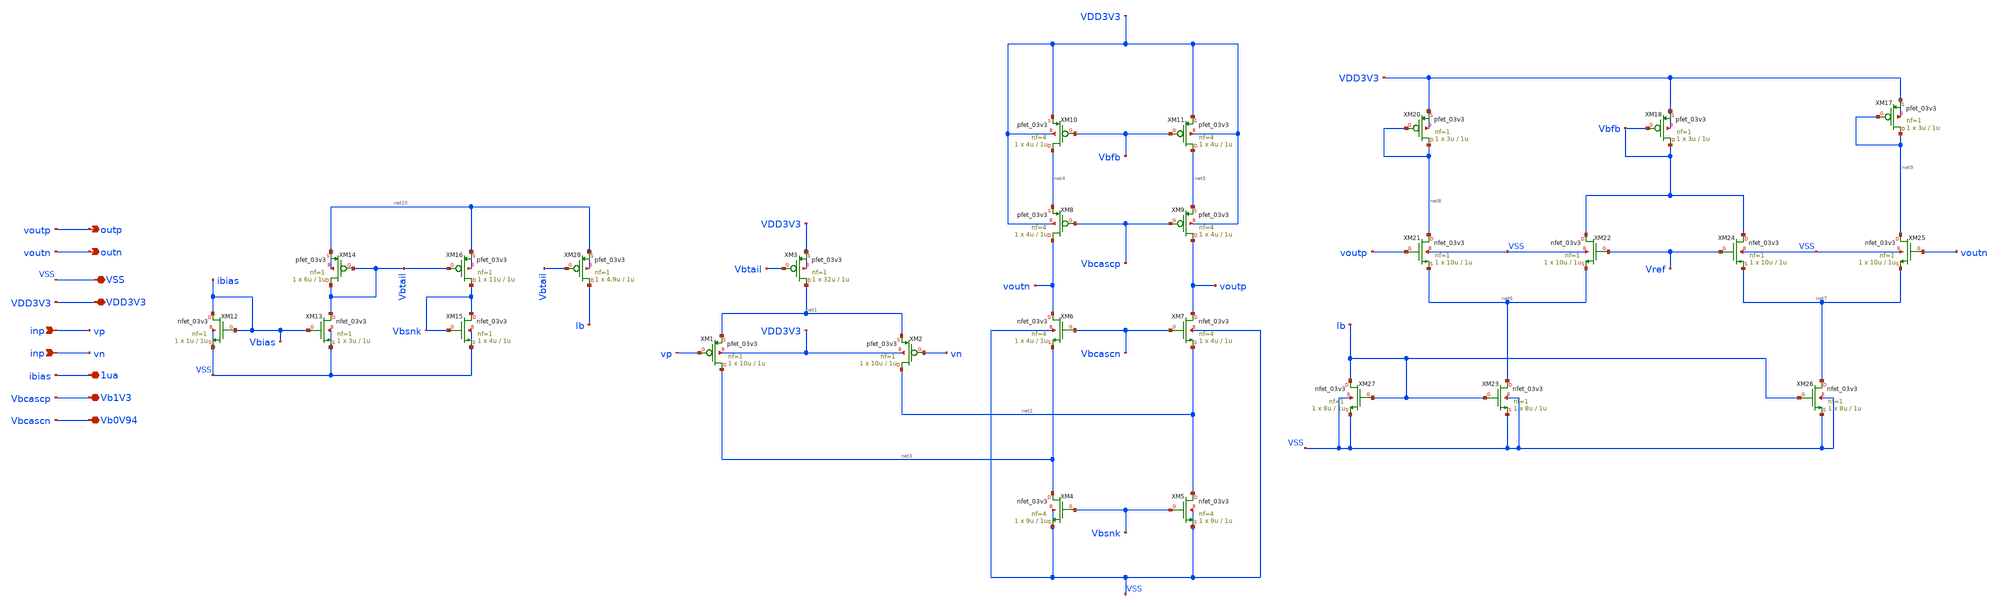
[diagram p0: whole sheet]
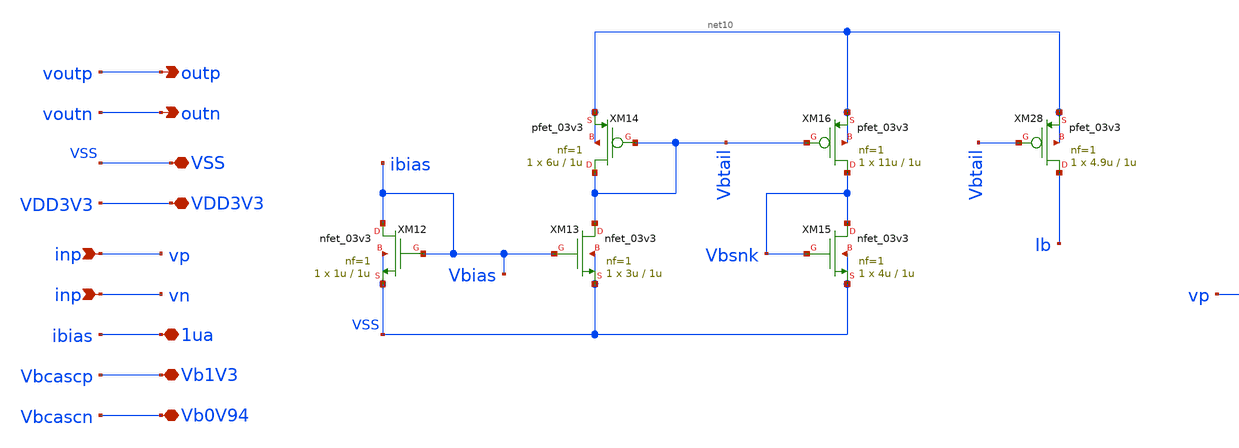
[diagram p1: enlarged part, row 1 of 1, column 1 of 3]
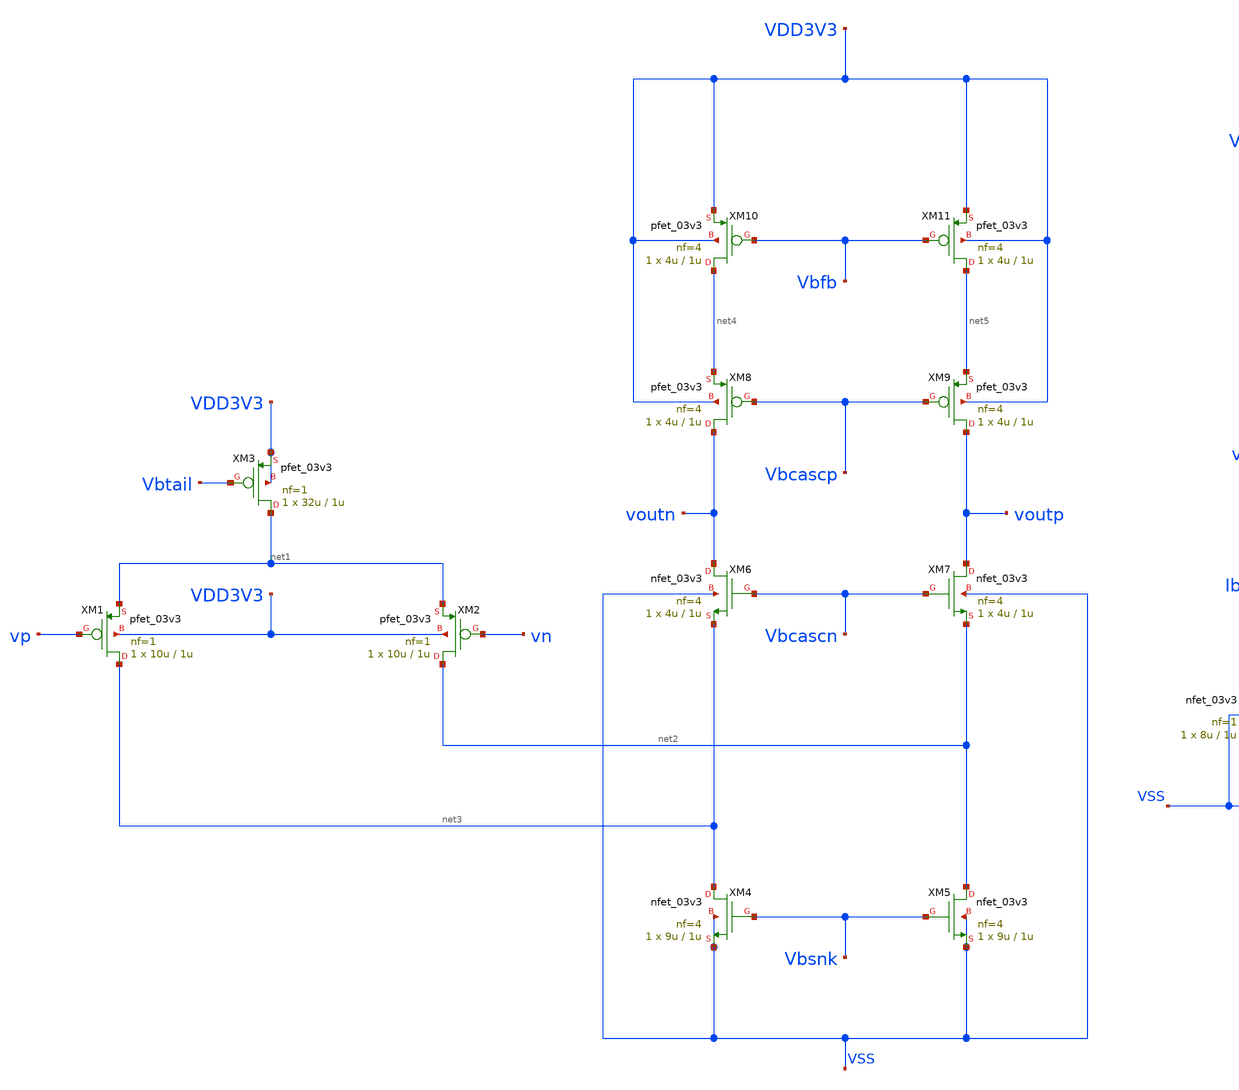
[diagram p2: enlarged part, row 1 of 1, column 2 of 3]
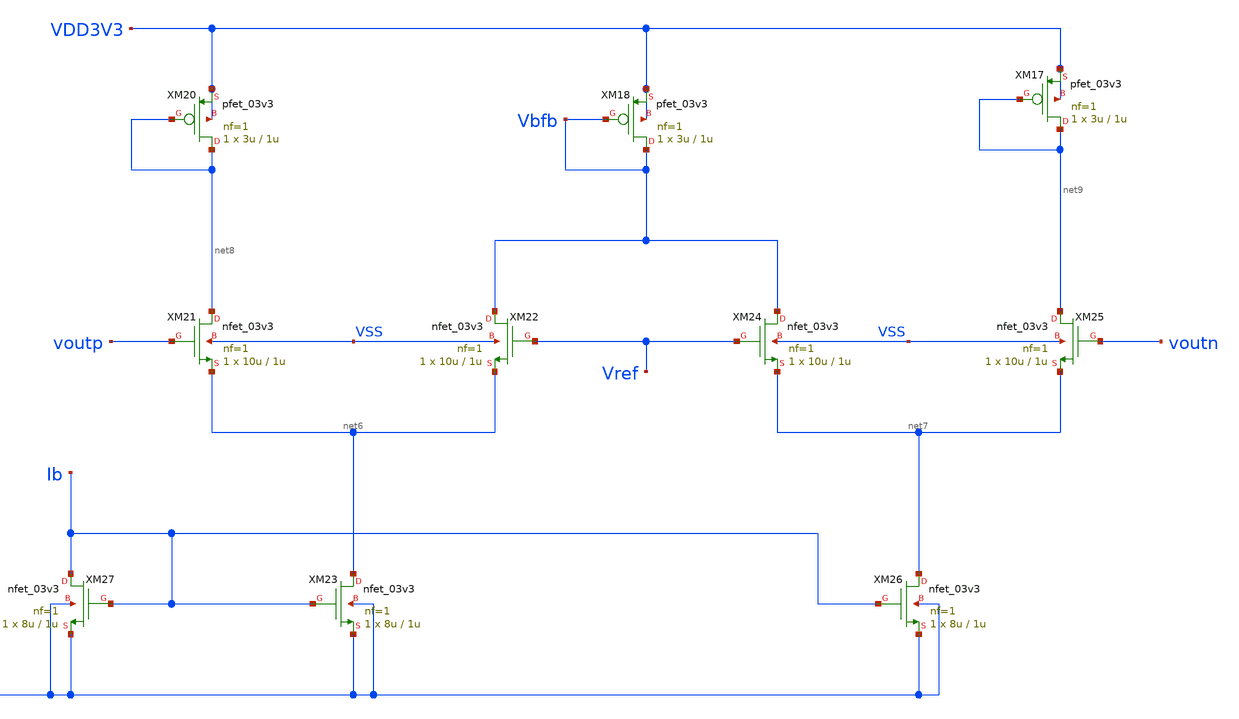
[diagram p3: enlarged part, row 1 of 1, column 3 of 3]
** sch_path: designs/libs/folded_cascode/folded_cascode_v2.sch
**.subckt folded_cascode_v2 outp outn VSS VDD3V3 inp inp 1ua Vb1V3 Vb0V94
*.opin outp
*.opin outn
*.iopin VSS
*.iopin VDD3V3
*.ipin inp
*.ipin inp
*.iopin 1ua
*.iopin Vb1V3
*.iopin Vb0V94
XM1 net3 vp net1 VDD3V3 pfet_03v3 L=1u W=10u nf=1 ad='int((nf+1)/2) * W/nf * 0.18u' as='int((nf+2)/2) * W/nf * 0.18u'
+ pd='2*int((nf+1)/2) * (W/nf + 0.18u)' ps='2*int((nf+2)/2) * (W/nf + 0.18u)' nrd='0.18u / W' nrs='0.18u / W'
+ sa=0 sb=0 sd=0 m=1
XM2 net2 vn net1 VDD3V3 pfet_03v3 L=1u W=10u nf=1 ad='int((nf+1)/2) * W/nf * 0.18u' as='int((nf+2)/2) * W/nf * 0.18u'
+ pd='2*int((nf+1)/2) * (W/nf + 0.18u)' ps='2*int((nf+2)/2) * (W/nf + 0.18u)' nrd='0.18u / W' nrs='0.18u / W'
+ sa=0 sb=0 sd=0 m=1
XM6 voutn Vbcascn net3 VSS nfet_03v3 L=1u W=4u nf=4 ad='int((nf+1)/2) * W/nf * 0.18u' as='int((nf+2)/2) * W/nf * 0.18u'
+ pd='2*int((nf+1)/2) * (W/nf + 0.18u)' ps='2*int((nf+2)/2) * (W/nf + 0.18u)' nrd='0.18u / W' nrs='0.18u / W'
+ sa=0 sb=0 sd=0 m=1
XM7 voutp Vbcascn net2 VSS nfet_03v3 L=1u W=4u nf=4 ad='int((nf+1)/2) * W/nf * 0.18u' as='int((nf+2)/2) * W/nf * 0.18u'
+ pd='2*int((nf+1)/2) * (W/nf + 0.18u)' ps='2*int((nf+2)/2) * (W/nf + 0.18u)' nrd='0.18u / W' nrs='0.18u / W'
+ sa=0 sb=0 sd=0 m=1
XM8 voutn Vbcascp net4 VDD3V3 pfet_03v3 L=1u W=4u nf=4 ad='int((nf+1)/2) * W/nf * 0.18u' as='int((nf+2)/2) * W/nf * 0.18u'
+ pd='2*int((nf+1)/2) * (W/nf + 0.18u)' ps='2*int((nf+2)/2) * (W/nf + 0.18u)' nrd='0.18u / W' nrs='0.18u / W'
+ sa=0 sb=0 sd=0 m=1
XM9 voutp Vbcascp net5 VDD3V3 pfet_03v3 L=1u W=4u nf=4 ad='int((nf+1)/2) * W/nf * 0.18u' as='int((nf+2)/2) * W/nf * 0.18u'
+ pd='2*int((nf+1)/2) * (W/nf + 0.18u)' ps='2*int((nf+2)/2) * (W/nf + 0.18u)' nrd='0.18u / W' nrs='0.18u / W'
+ sa=0 sb=0 sd=0 m=1
XM3 net1 Vbtail VDD3V3 VDD3V3 pfet_03v3 L=1u W=32u nf=1 ad='int((nf+1)/2) * W/nf * 0.18u' as='int((nf+2)/2) * W/nf * 0.18u'
+ pd='2*int((nf+1)/2) * (W/nf + 0.18u)' ps='2*int((nf+2)/2) * (W/nf + 0.18u)' nrd='0.18u / W' nrs='0.18u / W'
+ sa=0 sb=0 sd=0 m=1
XM4 net3 Vbsnk VSS VSS nfet_03v3 L=1u W=9u nf=4 ad='int((nf+1)/2) * W/nf * 0.18u' as='int((nf+2)/2) * W/nf * 0.18u'
+ pd='2*int((nf+1)/2) * (W/nf + 0.18u)' ps='2*int((nf+2)/2) * (W/nf + 0.18u)' nrd='0.18u / W' nrs='0.18u / W'
+ sa=0 sb=0 sd=0 m=1
XM5 net2 Vbsnk VSS VSS nfet_03v3 L=1u W=9u nf=4 ad='int((nf+1)/2) * W/nf * 0.18u' as='int((nf+2)/2) * W/nf * 0.18u'
+ pd='2*int((nf+1)/2) * (W/nf + 0.18u)' ps='2*int((nf+2)/2) * (W/nf + 0.18u)' nrd='0.18u / W' nrs='0.18u / W'
+ sa=0 sb=0 sd=0 m=1
XM10 net4 Vbfb VDD3V3 VDD3V3 pfet_03v3 L=1u W=4u nf=4 ad='int((nf+1)/2) * W/nf * 0.18u' as='int((nf+2)/2) * W/nf * 0.18u'
+ pd='2*int((nf+1)/2) * (W/nf + 0.18u)' ps='2*int((nf+2)/2) * (W/nf + 0.18u)' nrd='0.18u / W' nrs='0.18u / W'
+ sa=0 sb=0 sd=0 m=1
XM11 net5 Vbfb VDD3V3 VDD3V3 pfet_03v3 L=1u W=4u nf=4 ad='int((nf+1)/2) * W/nf * 0.18u' as='int((nf+2)/2) * W/nf * 0.18u'
+ pd='2*int((nf+1)/2) * (W/nf + 0.18u)' ps='2*int((nf+2)/2) * (W/nf + 0.18u)' nrd='0.18u / W' nrs='0.18u / W'
+ sa=0 sb=0 sd=0 m=1
XM20 net8 net8 VDD3V3 VDD3V3 pfet_03v3 L=1u W=3u nf=1 ad='int((nf+1)/2) * W/nf * 0.18u' as='int((nf+2)/2) * W/nf * 0.18u'
+ pd='2*int((nf+1)/2) * (W/nf + 0.18u)' ps='2*int((nf+2)/2) * (W/nf + 0.18u)' nrd='0.18u / W' nrs='0.18u / W'
+ sa=0 sb=0 sd=0 m=1
XM21 net8 voutp net6 VSS nfet_03v3 L=1u W=10u nf=1 ad='int((nf+1)/2) * W/nf * 0.18u' as='int((nf+2)/2) * W/nf * 0.18u'
+ pd='2*int((nf+1)/2) * (W/nf + 0.18u)' ps='2*int((nf+2)/2) * (W/nf + 0.18u)' nrd='0.18u / W' nrs='0.18u / W'
+ sa=0 sb=0 sd=0 m=1
XM22 Vbfb Vref net6 VSS nfet_03v3 L=1u W=10u nf=1 ad='int((nf+1)/2) * W/nf * 0.18u' as='int((nf+2)/2) * W/nf * 0.18u'
+ pd='2*int((nf+1)/2) * (W/nf + 0.18u)' ps='2*int((nf+2)/2) * (W/nf + 0.18u)' nrd='0.18u / W' nrs='0.18u / W'
+ sa=0 sb=0 sd=0 m=1
XM23 net6 Ib VSS VSS nfet_03v3 L=1u W=8u nf=1 ad='int((nf+1)/2) * W/nf * 0.18u' as='int((nf+2)/2) * W/nf * 0.18u'
+ pd='2*int((nf+1)/2) * (W/nf + 0.18u)' ps='2*int((nf+2)/2) * (W/nf + 0.18u)' nrd='0.18u / W' nrs='0.18u / W'
+ sa=0 sb=0 sd=0 m=1
XM24 Vbfb Vref net7 VSS nfet_03v3 L=1u W=10u nf=1 ad='int((nf+1)/2) * W/nf * 0.18u' as='int((nf+2)/2) * W/nf * 0.18u'
+ pd='2*int((nf+1)/2) * (W/nf + 0.18u)' ps='2*int((nf+2)/2) * (W/nf + 0.18u)' nrd='0.18u / W' nrs='0.18u / W'
+ sa=0 sb=0 sd=0 m=1
XM25 net9 voutn net7 VSS nfet_03v3 L=1u W=10u nf=1 ad='int((nf+1)/2) * W/nf * 0.18u' as='int((nf+2)/2) * W/nf * 0.18u'
+ pd='2*int((nf+1)/2) * (W/nf + 0.18u)' ps='2*int((nf+2)/2) * (W/nf + 0.18u)' nrd='0.18u / W' nrs='0.18u / W'
+ sa=0 sb=0 sd=0 m=1
XM26 net7 Ib VSS VSS nfet_03v3 L=1u W=8u nf=1 ad='int((nf+1)/2) * W/nf * 0.18u' as='int((nf+2)/2) * W/nf * 0.18u'
+ pd='2*int((nf+1)/2) * (W/nf + 0.18u)' ps='2*int((nf+2)/2) * (W/nf + 0.18u)' nrd='0.18u / W' nrs='0.18u / W'
+ sa=0 sb=0 sd=0 m=1
XM27 Ib Ib VSS VSS nfet_03v3 L=1u W=8u nf=1 ad='int((nf+1)/2) * W/nf * 0.18u' as='int((nf+2)/2) * W/nf * 0.18u'
+ pd='2*int((nf+1)/2) * (W/nf + 0.18u)' ps='2*int((nf+2)/2) * (W/nf + 0.18u)' nrd='0.18u / W' nrs='0.18u / W'
+ sa=0 sb=0 sd=0 m=1
XM12 Vbias Vbias VSS VSS nfet_03v3 L=1u W=1u nf=1 ad='int((nf+1)/2) * W/nf * 0.18u' as='int((nf+2)/2) * W/nf * 0.18u'
+ pd='2*int((nf+1)/2) * (W/nf + 0.18u)' ps='2*int((nf+2)/2) * (W/nf + 0.18u)' nrd='0.18u / W' nrs='0.18u / W'
+ sa=0 sb=0 sd=0 m=1
XM13 Vbtail Vbias VSS VSS nfet_03v3 L=1u W=3u nf=1 ad='int((nf+1)/2) * W/nf * 0.18u' as='int((nf+2)/2) * W/nf * 0.18u'
+ pd='2*int((nf+1)/2) * (W/nf + 0.18u)' ps='2*int((nf+2)/2) * (W/nf + 0.18u)' nrd='0.18u / W' nrs='0.18u / W'
+ sa=0 sb=0 sd=0 m=1
XM14 Vbtail Vbtail net10 net10 pfet_03v3 L=1u W=6u nf=1 ad='int((nf+1)/2) * W/nf * 0.18u' as='int((nf+2)/2) * W/nf * 0.18u'
+ pd='2*int((nf+1)/2) * (W/nf + 0.18u)' ps='2*int((nf+2)/2) * (W/nf + 0.18u)' nrd='0.18u / W' nrs='0.18u / W'
+ sa=0 sb=0 sd=0 m=1
XM15 Vbsnk Vbsnk VSS VSS nfet_03v3 L=1u W=4u nf=1 ad='int((nf+1)/2) * W/nf * 0.18u' as='int((nf+2)/2) * W/nf * 0.18u'
+ pd='2*int((nf+1)/2) * (W/nf + 0.18u)' ps='2*int((nf+2)/2) * (W/nf + 0.18u)' nrd='0.18u / W' nrs='0.18u / W'
+ sa=0 sb=0 sd=0 m=1
XM16 Vbsnk Vbtail net10 net10 pfet_03v3 L=1u W=11u nf=1 ad='int((nf+1)/2) * W/nf * 0.18u' as='int((nf+2)/2) * W/nf * 0.18u'
+ pd='2*int((nf+1)/2) * (W/nf + 0.18u)' ps='2*int((nf+2)/2) * (W/nf + 0.18u)' nrd='0.18u / W' nrs='0.18u / W'
+ sa=0 sb=0 sd=0 m=1
XM17 net9 net9 VDD3V3 VDD3V3 pfet_03v3 L=1u W=3u nf=1 ad='int((nf+1)/2) * W/nf * 0.18u' as='int((nf+2)/2) * W/nf * 0.18u'
+ pd='2*int((nf+1)/2) * (W/nf + 0.18u)' ps='2*int((nf+2)/2) * (W/nf + 0.18u)' nrd='0.18u / W' nrs='0.18u / W'
+ sa=0 sb=0 sd=0 m=1
XM18 Vbfb Vbfb VDD3V3 VDD3V3 pfet_03v3 L=1u W=3u nf=1 ad='int((nf+1)/2) * W/nf * 0.18u' as='int((nf+2)/2) * W/nf * 0.18u'
+ pd='2*int((nf+1)/2) * (W/nf + 0.18u)' ps='2*int((nf+2)/2) * (W/nf + 0.18u)' nrd='0.18u / W' nrs='0.18u / W'
+ sa=0 sb=0 sd=0 m=1
XM28 Ib Vbtail net10 net10 pfet_03v3 L=1u W=4.9u nf=1 ad='int((nf+1)/2) * W/nf * 0.18u' as='int((nf+2)/2) * W/nf * 0.18u'
+ pd='2*int((nf+1)/2) * (W/nf + 0.18u)' ps='2*int((nf+2)/2) * (W/nf + 0.18u)' nrd='0.18u / W' nrs='0.18u / W'
+ sa=0 sb=0 sd=0 m=1
**.ends
.end
